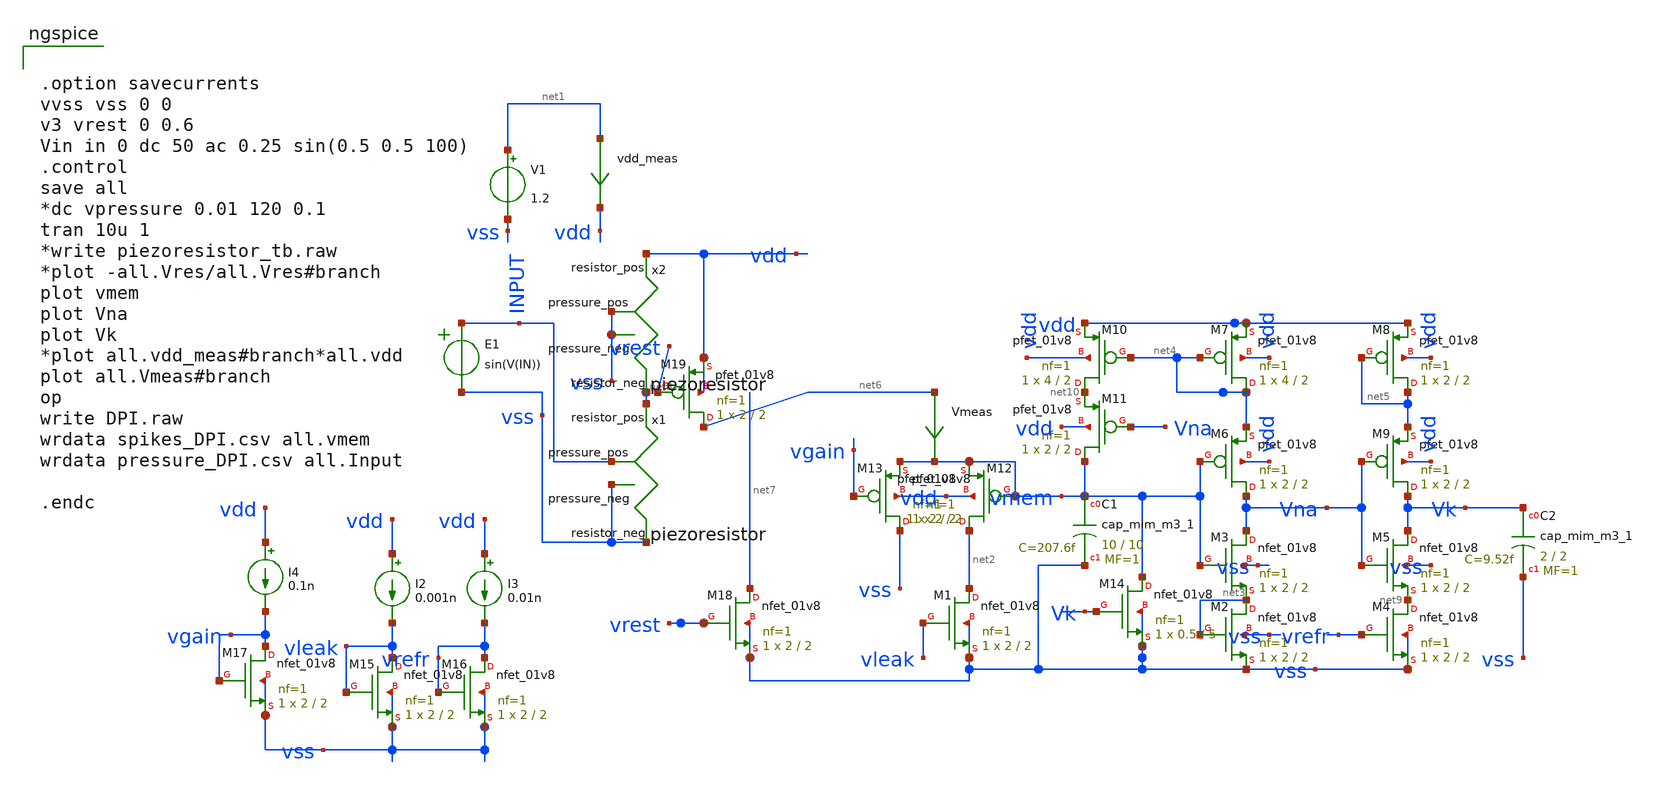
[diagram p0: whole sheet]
** sch_path: circuits/DPI_neuron.sch
* Copyright 2020 Stefan Frederik Schippers
* Licensed under the Apache License, Version 2.0 (the "License");
* you may not use this file except in compliance with the License.
* You may obtain a copy of the License at
* https://www.apache.org/licenses/LICENSE-2.0
* Unless required by applicable law or agreed to in writing, software
* distributed under the License is distributed on an "AS IS" BASIS,
* WITHOUT WARRANTIES OR CONDITIONS OF ANY KIND, either express or implied.
* See the License for the specific language governing permissions and
* limitations under the License.
**.subckt DPI_neuron
E1 INPUT vss VOL=' sin(V(IN)) '
Vmeas net6 vmem 0
.save i(vmeas)
vdd_meas net1 vdd 0
.save i(vdd_meas)
V1 net1 vss 1.2
XM1 net2 vleak vss vss sky130_fd_pr__nfet_01v8 L=2 W=2 nf=1 ad='int((nf+1)/2) * W/nf * 0.29' as='int((nf+2)/2) * W/nf * 0.29'
+ pd='2*int((nf+1)/2) * (W/nf + 0.29)' ps='2*int((nf+2)/2) * (W/nf + 0.29)' nrd='0.29 / W' nrs='0.29 / W'
+ sa=0 sb=0 sd=0 mult=1 m=1
XM2 net3 net3 vss vss sky130_fd_pr__nfet_01v8 L=2 W=2 nf=1 ad='int((nf+1)/2) * W/nf * 0.29' as='int((nf+2)/2) * W/nf * 0.29'
+ pd='2*int((nf+1)/2) * (W/nf + 0.29)' ps='2*int((nf+2)/2) * (W/nf + 0.29)' nrd='0.29 / W' nrs='0.29 / W'
+ sa=0 sb=0 sd=0 mult=1 m=1
XM3 Vna vmem net3 vss sky130_fd_pr__nfet_01v8 L=2 W=2 nf=1 ad='int((nf+1)/2) * W/nf * 0.29' as='int((nf+2)/2) * W/nf * 0.29'
+ pd='2*int((nf+1)/2) * (W/nf + 0.29)' ps='2*int((nf+2)/2) * (W/nf + 0.29)' nrd='0.29 / W' nrs='0.29 / W'
+ sa=0 sb=0 sd=0 mult=1 m=1
XC1 vmem vss sky130_fd_pr__cap_mim_m3_1 W=10 L=10 MF=1 m=1
XC2 Vk vss sky130_fd_pr__cap_mim_m3_1 W=2 L=2 MF=1 m=1
XM14 vmem Vk vss vss sky130_fd_pr__nfet_01v8 L=5 W=0.5 nf=1 ad='int((nf+1)/2) * W/nf * 0.29' as='int((nf+2)/2) * W/nf * 0.29'
+ pd='2*int((nf+1)/2) * (W/nf + 0.29)' ps='2*int((nf+2)/2) * (W/nf + 0.29)' nrd='0.29 / W' nrs='0.29 / W'
+ sa=0 sb=0 sd=0 mult=1 m=1
XM4 net9 vrefr vss vss sky130_fd_pr__nfet_01v8 L=2 W=2 nf=1 ad='int((nf+1)/2) * W/nf * 0.29' as='int((nf+2)/2) * W/nf * 0.29'
+ pd='2*int((nf+1)/2) * (W/nf + 0.29)' ps='2*int((nf+2)/2) * (W/nf + 0.29)' nrd='0.29 / W' nrs='0.29 / W'
+ sa=0 sb=0 sd=0 mult=1 m=1
XM5 Vk Vna net9 vss sky130_fd_pr__nfet_01v8 L=2 W=2 nf=1 ad='int((nf+1)/2) * W/nf * 0.29' as='int((nf+2)/2) * W/nf * 0.29'
+ pd='2*int((nf+1)/2) * (W/nf + 0.29)' ps='2*int((nf+2)/2) * (W/nf + 0.29)' nrd='0.29 / W' nrs='0.29 / W'
+ sa=0 sb=0 sd=0 mult=1 m=1
I2 vdd vleak 0.001n
XM15 vleak vleak vss vss sky130_fd_pr__nfet_01v8 L=2 W=2 nf=1 ad='int((nf+1)/2) * W/nf * 0.29' as='int((nf+2)/2) * W/nf * 0.29'
+ pd='2*int((nf+1)/2) * (W/nf + 0.29)' ps='2*int((nf+2)/2) * (W/nf + 0.29)' nrd='0.29 / W' nrs='0.29 / W'
+ sa=0 sb=0 sd=0 mult=1 m=1
I3 vdd vrefr 0.01n
XM16 vrefr vrefr vss vss sky130_fd_pr__nfet_01v8 L=2 W=2 nf=1 ad='int((nf+1)/2) * W/nf * 0.29' as='int((nf+2)/2) * W/nf * 0.29'
+ pd='2*int((nf+1)/2) * (W/nf + 0.29)' ps='2*int((nf+2)/2) * (W/nf + 0.29)' nrd='0.29 / W' nrs='0.29 / W'
+ sa=0 sb=0 sd=0 mult=1 m=1
I4 vdd vgain 0.1n
XM17 vgain vgain vss vss sky130_fd_pr__nfet_01v8 L=2 W=2 nf=1 ad='int((nf+1)/2) * W/nf * 0.29' as='int((nf+2)/2) * W/nf * 0.29'
+ pd='2*int((nf+1)/2) * (W/nf + 0.29)' ps='2*int((nf+2)/2) * (W/nf + 0.29)' nrd='0.29 / W' nrs='0.29 / W'
+ sa=0 sb=0 sd=0 mult=1 m=1
XM6 Vna vmem net4 vdd sky130_fd_pr__pfet_01v8 L=2 W=2 nf=1 ad='int((nf+1)/2) * W/nf * 0.29' as='int((nf+2)/2) * W/nf * 0.29'
+ pd='2*int((nf+1)/2) * (W/nf + 0.29)' ps='2*int((nf+2)/2) * (W/nf + 0.29)' nrd='0.29 / W' nrs='0.29 / W'
+ sa=0 sb=0 sd=0 mult=1 m=1
XM7 net4 net4 vdd vdd sky130_fd_pr__pfet_01v8 L=2 W=4 nf=1 ad='int((nf+1)/2) * W/nf * 0.29' as='int((nf+2)/2) * W/nf * 0.29'
+ pd='2*int((nf+1)/2) * (W/nf + 0.29)' ps='2*int((nf+2)/2) * (W/nf + 0.29)' nrd='0.29 / W' nrs='0.29 / W'
+ sa=0 sb=0 sd=0 mult=1 m=1
XM8 net5 net5 vdd vdd sky130_fd_pr__pfet_01v8 L=2 W=2 nf=1 ad='int((nf+1)/2) * W/nf * 0.29' as='int((nf+2)/2) * W/nf * 0.29'
+ pd='2*int((nf+1)/2) * (W/nf + 0.29)' ps='2*int((nf+2)/2) * (W/nf + 0.29)' nrd='0.29 / W' nrs='0.29 / W'
+ sa=0 sb=0 sd=0 mult=1 m=1
XM9 Vk Vna net5 vdd sky130_fd_pr__pfet_01v8 L=2 W=2 nf=1 ad='int((nf+1)/2) * W/nf * 0.29' as='int((nf+2)/2) * W/nf * 0.29'
+ pd='2*int((nf+1)/2) * (W/nf + 0.29)' ps='2*int((nf+2)/2) * (W/nf + 0.29)' nrd='0.29 / W' nrs='0.29 / W'
+ sa=0 sb=0 sd=0 mult=1 m=1
XM10 net10 net4 vdd vdd sky130_fd_pr__pfet_01v8 L=2 W=4 nf=1 ad='int((nf+1)/2) * W/nf * 0.29' as='int((nf+2)/2) * W/nf * 0.29'
+ pd='2*int((nf+1)/2) * (W/nf + 0.29)' ps='2*int((nf+2)/2) * (W/nf + 0.29)' nrd='0.29 / W' nrs='0.29 / W'
+ sa=0 sb=0 sd=0 mult=1 m=1
XM11 vmem Vna net10 vdd sky130_fd_pr__pfet_01v8 L=2 W=2 nf=1 ad='int((nf+1)/2) * W/nf * 0.29' as='int((nf+2)/2) * W/nf * 0.29'
+ pd='2*int((nf+1)/2) * (W/nf + 0.29)' ps='2*int((nf+2)/2) * (W/nf + 0.29)' nrd='0.29 / W' nrs='0.29 / W'
+ sa=0 sb=0 sd=0 mult=1 m=1
XM12 net2 vmem vmem vdd sky130_fd_pr__pfet_01v8 L=2 W=2 nf=1 ad='int((nf+1)/2) * W/nf * 0.29' as='int((nf+2)/2) * W/nf * 0.29'
+ pd='2*int((nf+1)/2) * (W/nf + 0.29)' ps='2*int((nf+2)/2) * (W/nf + 0.29)' nrd='0.29 / W' nrs='0.29 / W'
+ sa=0 sb=0 sd=0 mult=1 m=1
XM13 vss vgain vmem vdd sky130_fd_pr__pfet_01v8 L=2 W=2 nf=1 ad='int((nf+1)/2) * W/nf * 0.29' as='int((nf+2)/2) * W/nf * 0.29'
+ pd='2*int((nf+1)/2) * (W/nf + 0.29)' ps='2*int((nf+2)/2) * (W/nf + 0.29)' nrd='0.29 / W' nrs='0.29 / W'
+ sa=0 sb=0 sd=0 mult=1 m=1
x2 vss vss vdd net8 piezoresistor
XM18 net7 vrest vss vss sky130_fd_pr__nfet_01v8 L=2 W=2 nf=1 ad='int((nf+1)/2) * W/nf * 0.29' as='int((nf+2)/2) * W/nf * 0.29'
+ pd='2*int((nf+1)/2) * (W/nf + 0.29)' ps='2*int((nf+2)/2) * (W/nf + 0.29)' nrd='0.29 / W' nrs='0.29 / W'
+ sa=0 sb=0 sd=0 mult=1 m=1
x1 INPUT vss net8 vss piezoresistor
XM19 net6 vrest vdd vdd sky130_fd_pr__pfet_01v8 L=2 W=2 nf=1 ad='int((nf+1)/2) * W/nf * 0.29' as='int((nf+2)/2) * W/nf * 0.29'
+ pd='2*int((nf+1)/2) * (W/nf + 0.29)' ps='2*int((nf+2)/2) * (W/nf + 0.29)' nrd='0.29 / W' nrs='0.29 / W'
+ sa=0 sb=0 sd=0 mult=1 m=1
**** begin user architecture code


.option savecurrents
vvss vss 0 0
v3 vrest 0 0.6
Vin in 0 dc 50 ac 0.25 sin(0.5 0.5 100)
.control
save all
*dc vpressure 0.01 120 0.1
tran 10u 1
*write piezoresistor_tb.raw
*plot -all.Vres/all.Vres#branch
plot vmem
plot Vna
plot Vk
*plot all.vdd_meas#branch*all.vdd
plot all.Vmeas#branch
op
write DPI.raw
wrdata spikes_DPI.csv all.vmem
wrdata pressure_DPI.csv all.Input

.endc


 .lib $::SKYWATER_MODELS/models/sky130.lib.spice tt

.param mc_mm_switch=0
.param mc_pr_switch=1


**** end user architecture code
**.ends

* expanding   symbol:  /home/mast/Progetti/Telluride2021/sky130_TAC3/circuits/piezoresistor.sym # of
*+ pins=4
** sym_path: circuits/piezoresistor.sym
** sch_path: circuits/piezoresistor.sch
.subckt piezoresistor pressure_pos pressure_neg resistor_pos resistor_neg
*.ipin pressure_pos
*.ipin pressure_neg
*.iopin resistor_pos
*.iopin resistor_neg
Broot sqrtp 0 V = sqrt(v(pressure_pos,pressure_neg))
Bres res 0 V = 106*(50/v(sqrtp)-1)*exp(-0.328*v(sqrtp))+15
Brvar resistor_pos resistor_neg I = V(resistor_pos,resistor_neg)/V(res)
.ends

.end
